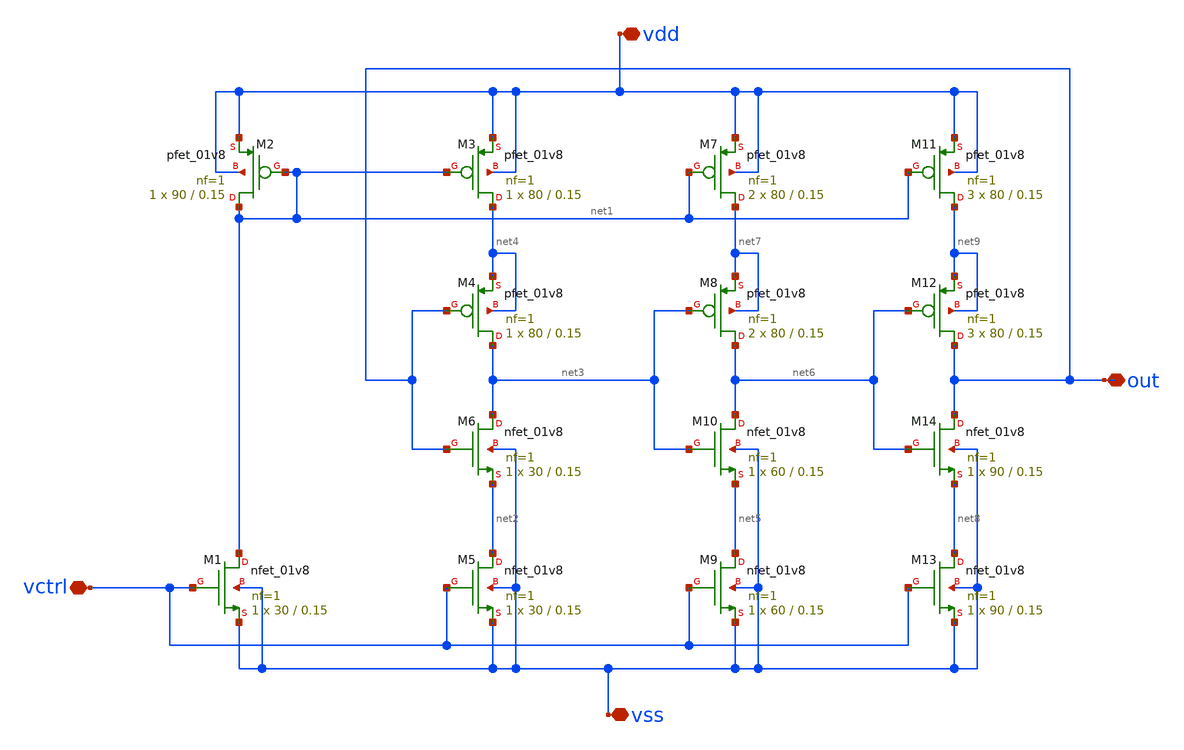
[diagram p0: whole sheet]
** sch_path: xschem01/vco/vco.sch
**.subckt vco vdd vss out vctrl
*.iopin vdd
*.iopin vss
*.iopin out
*.iopin vctrl
XM1 net1 vctrl vss vss sky130_fd_pr__nfet_01v8 L=0.15 W=30 nf=1 ad='int((nf+1)/2) * W/nf * 0.29' as='int((nf+2)/2) * W/nf * 0.29'
+ pd='2*int((nf+1)/2) * (W/nf + 0.29)' ps='2*int((nf+2)/2) * (W/nf + 0.29)' nrd='0.29 / W' nrs='0.29 / W'
+ sa=0 sb=0 sd=0 mult=1 m=1
XM2 net1 net1 vdd vdd sky130_fd_pr__pfet_01v8 L=0.15 W=90 nf=1 ad='int((nf+1)/2) * W/nf * 0.29' as='int((nf+2)/2) * W/nf * 0.29'
+ pd='2*int((nf+1)/2) * (W/nf + 0.29)' ps='2*int((nf+2)/2) * (W/nf + 0.29)' nrd='0.29 / W' nrs='0.29 / W'
+ sa=0 sb=0 sd=0 mult=1 m=1
XM3 net4 net1 vdd vdd sky130_fd_pr__pfet_01v8 L=0.15 W=80 nf=1 ad='int((nf+1)/2) * W/nf * 0.29' as='int((nf+2)/2) * W/nf * 0.29'
+ pd='2*int((nf+1)/2) * (W/nf + 0.29)' ps='2*int((nf+2)/2) * (W/nf + 0.29)' nrd='0.29 / W' nrs='0.29 / W'
+ sa=0 sb=0 sd=0 mult=1 m=1
XM4 net3 out net4 net4 sky130_fd_pr__pfet_01v8 L=0.15 W=80 nf=1 ad='int((nf+1)/2) * W/nf * 0.29' as='int((nf+2)/2) * W/nf * 0.29'
+ pd='2*int((nf+1)/2) * (W/nf + 0.29)' ps='2*int((nf+2)/2) * (W/nf + 0.29)' nrd='0.29 / W' nrs='0.29 / W'
+ sa=0 sb=0 sd=0 mult=1 m=1
XM5 net2 vctrl vss vss sky130_fd_pr__nfet_01v8 L=0.15 W=30 nf=1 ad='int((nf+1)/2) * W/nf * 0.29' as='int((nf+2)/2) * W/nf * 0.29'
+ pd='2*int((nf+1)/2) * (W/nf + 0.29)' ps='2*int((nf+2)/2) * (W/nf + 0.29)' nrd='0.29 / W' nrs='0.29 / W'
+ sa=0 sb=0 sd=0 mult=1 m=1
XM6 net3 out net2 vss sky130_fd_pr__nfet_01v8 L=0.15 W=30 nf=1 ad='int((nf+1)/2) * W/nf * 0.29' as='int((nf+2)/2) * W/nf * 0.29'
+ pd='2*int((nf+1)/2) * (W/nf + 0.29)' ps='2*int((nf+2)/2) * (W/nf + 0.29)' nrd='0.29 / W' nrs='0.29 / W'
+ sa=0 sb=0 sd=0 mult=1 m=1
XM7 net7 net1 vdd vdd sky130_fd_pr__pfet_01v8 L=0.15 W=80 nf=1 ad='int((nf+1)/2) * W/nf * 0.29' as='int((nf+2)/2) * W/nf * 0.29'
+ pd='2*int((nf+1)/2) * (W/nf + 0.29)' ps='2*int((nf+2)/2) * (W/nf + 0.29)' nrd='0.29 / W' nrs='0.29 / W'
+ sa=0 sb=0 sd=0 mult=2 m=2
XM8 net6 net3 net7 net7 sky130_fd_pr__pfet_01v8 L=0.15 W=80 nf=1 ad='int((nf+1)/2) * W/nf * 0.29' as='int((nf+2)/2) * W/nf * 0.29'
+ pd='2*int((nf+1)/2) * (W/nf + 0.29)' ps='2*int((nf+2)/2) * (W/nf + 0.29)' nrd='0.29 / W' nrs='0.29 / W'
+ sa=0 sb=0 sd=0 mult=2 m=2
XM9 net5 vctrl vss vss sky130_fd_pr__nfet_01v8 L=0.15 W=60 nf=1 ad='int((nf+1)/2) * W/nf * 0.29' as='int((nf+2)/2) * W/nf * 0.29'
+ pd='2*int((nf+1)/2) * (W/nf + 0.29)' ps='2*int((nf+2)/2) * (W/nf + 0.29)' nrd='0.29 / W' nrs='0.29 / W'
+ sa=0 sb=0 sd=0 mult=1 m=1
XM10 net6 net3 net5 vss sky130_fd_pr__nfet_01v8 L=0.15 W=60 nf=1 ad='int((nf+1)/2) * W/nf * 0.29' as='int((nf+2)/2) * W/nf * 0.29'
+ pd='2*int((nf+1)/2) * (W/nf + 0.29)' ps='2*int((nf+2)/2) * (W/nf + 0.29)' nrd='0.29 / W' nrs='0.29 / W'
+ sa=0 sb=0 sd=0 mult=1 m=1
XM11 net9 net1 vdd vdd sky130_fd_pr__pfet_01v8 L=0.15 W=80 nf=1 ad='int((nf+1)/2) * W/nf * 0.29' as='int((nf+2)/2) * W/nf * 0.29'
+ pd='2*int((nf+1)/2) * (W/nf + 0.29)' ps='2*int((nf+2)/2) * (W/nf + 0.29)' nrd='0.29 / W' nrs='0.29 / W'
+ sa=0 sb=0 sd=0 mult=3 m=3
XM12 out net6 net9 net9 sky130_fd_pr__pfet_01v8 L=0.15 W=80 nf=1 ad='int((nf+1)/2) * W/nf * 0.29' as='int((nf+2)/2) * W/nf * 0.29'
+ pd='2*int((nf+1)/2) * (W/nf + 0.29)' ps='2*int((nf+2)/2) * (W/nf + 0.29)' nrd='0.29 / W' nrs='0.29 / W'
+ sa=0 sb=0 sd=0 mult=3 m=3
XM13 net8 vctrl vss vss sky130_fd_pr__nfet_01v8 L=0.15 W=90 nf=1 ad='int((nf+1)/2) * W/nf * 0.29' as='int((nf+2)/2) * W/nf * 0.29'
+ pd='2*int((nf+1)/2) * (W/nf + 0.29)' ps='2*int((nf+2)/2) * (W/nf + 0.29)' nrd='0.29 / W' nrs='0.29 / W'
+ sa=0 sb=0 sd=0 mult=1 m=1
XM14 out net6 net8 vss sky130_fd_pr__nfet_01v8 L=0.15 W=90 nf=1 ad='int((nf+1)/2) * W/nf * 0.29' as='int((nf+2)/2) * W/nf * 0.29'
+ pd='2*int((nf+1)/2) * (W/nf + 0.29)' ps='2*int((nf+2)/2) * (W/nf + 0.29)' nrd='0.29 / W' nrs='0.29 / W'
+ sa=0 sb=0 sd=0 mult=1 m=1
**.ends
.end
